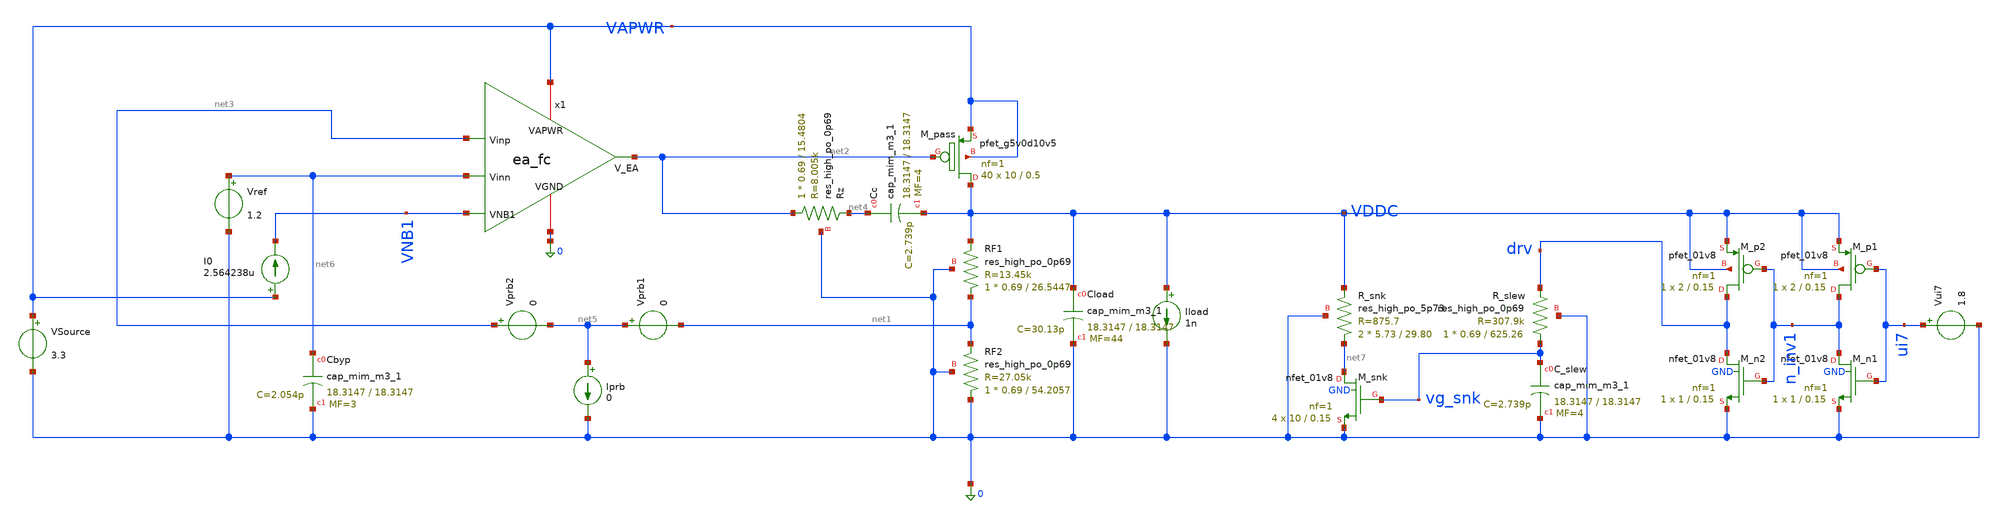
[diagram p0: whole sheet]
** sch_path: designs/bgr_ldo/ldo/ldo_core_withoutbgr_tb.sch
**.subckt ldo_core_withoutbgr_tb
XM_pass VDDC net2 VAPWR VAPWR sky130_fd_pr__pfet_g5v0d10v5 L=0.5 W=10 nf=1 ad='int((1 + 1)/2) * 10 / 1 * 0.29'
+ as='int((1 + 2)/2) * 10 / 1 * 0.29' pd='2*int((1 + 1)/2) * (10 / 1 + 0.29)' ps='2*int((1 + 2)/2) * (10 / 1 + 0.29)'
+ nrd='0.29 / 10 ' nrs='0.29 / 10 ' sa=0 sb=0 sd=0 mult=40 m=40
VSource VAPWR 0 3.3
x1 VAPWR net2 net3 net6 VNB1 0 ea_fc
Iload VDDC 0 1n
XRF1 net1 VDDC 0 sky130_fd_pr__res_high_po_0p69 L=26.5447 mult=1 m=1
XRF2 0 net1 0 sky130_fd_pr__res_high_po_0p69 L=54.2057 mult=1 m=1
XRz net2 net4 0 sky130_fd_pr__res_high_po_0p69 L=15.4804 mult=1 m=1
XCload VDDC 0 sky130_fd_pr__cap_mim_m3_1 W=18.3147 L=18.3147 MF=44 m=44
XCc net4 VDDC sky130_fd_pr__cap_mim_m3_1 W=18.3147 L=18.3147 MF=4 m=4
Vprb1 net5 net1 0
Vprb2 net3 net5 0
Iprb net5 0 0
XCbyp net6 0 sky130_fd_pr__cap_mim_m3_1 W=18.3147 L=18.3147 MF=3 m=3
XM_snk net7 vg_snk 0 GND sky130_fd_pr__nfet_01v8 L=0.15 W=10 nf=1 ad='int((1 + 1)/2) * 10 / 1 * 0.29'
+ as='int((1 + 2)/2) * 10 / 1 * 0.29' pd='2*int((1 + 1)/2) * (10 / 1 + 0.29)' ps='2*int((1 + 2)/2) * (10 / 1 + 0.29)'
+ nrd='0.29 / 10 ' nrs='0.29 / 10 ' sa=0 sb=0 sd=0 mult=4 m=4
Vui7 ui7 0 1.8
XR_slew vg_snk drv 0 sky130_fd_pr__res_high_po_0p69 L=625.26 mult=1 m=1
XC_slew vg_snk 0 sky130_fd_pr__cap_mim_m3_1 W=18.3147 L=18.3147 MF=4 m=4
XM_n1 n_inv1 ui7 0 GND sky130_fd_pr__nfet_01v8 L=0.15 W=1 nf=1 ad='int((1 + 1)/2) * 1 / 1 * 0.29' as='int((1 + 2)/2) * 1 / 1 * 0.29'
+ pd='2*int((1 + 1)/2) * (1 / 1 + 0.29)' ps='2*int((1 + 2)/2) * (1 / 1 + 0.29)' nrd='0.29 / 1 ' nrs='0.29 / 1 '
+ sa=0 sb=0 sd=0 mult=1 m=1
XM_p1 n_inv1 ui7 VDDC VDDC sky130_fd_pr__pfet_01v8 L=0.15 W=2 nf=1 ad='int((1 + 1)/2) * 2 / 1 * 0.29'
+ as='int((1 + 2)/2) * 2 / 1 * 0.29' pd='2*int((1 + 1)/2) * (2 / 1 + 0.29)' ps='2*int((1 + 2)/2) * (2 / 1 + 0.29)'
+ nrd='0.29 / 2 ' nrs='0.29 / 2 ' sa=0 sb=0 sd=0 mult=1 m=1
XM_n2 drv n_inv1 0 GND sky130_fd_pr__nfet_01v8 L=0.15 W=1 nf=1 ad='int((1 + 1)/2) * 1 / 1 * 0.29' as='int((1 + 2)/2) * 1 / 1 * 0.29'
+ pd='2*int((1 + 1)/2) * (1 / 1 + 0.29)' ps='2*int((1 + 2)/2) * (1 / 1 + 0.29)' nrd='0.29 / 1 ' nrs='0.29 / 1 '
+ sa=0 sb=0 sd=0 mult=1 m=1
XM_p2 drv n_inv1 VDDC VDDC sky130_fd_pr__pfet_01v8 L=0.15 W=2 nf=1 ad='int((1 + 1)/2) * 2 / 1 * 0.29'
+ as='int((1 + 2)/2) * 2 / 1 * 0.29' pd='2*int((1 + 1)/2) * (2 / 1 + 0.29)' ps='2*int((1 + 2)/2) * (2 / 1 + 0.29)'
+ nrd='0.29 / 2 ' nrs='0.29 / 2 ' sa=0 sb=0 sd=0 mult=1 m=1
XR_snk net7 VDDC 0 sky130_fd_pr__res_high_po_5p73 L=29.80 mult=2 m=2
Vref net6 0 1.2
I0 VAPWR VNB1 2.564238u
**** begin user architecture code

** opencircuitdesign pdks install
.lib $::SKYWATER_MODELS/sky130.lib.spice tt



.save all
.control
set wr_singlescale
tran 10n 40u 0 10n uic
wrdata failsafe_startup.txt v(VDDC) v(net2) v(VNB1)
.endc

**** end user architecture code
**.ends
.end
